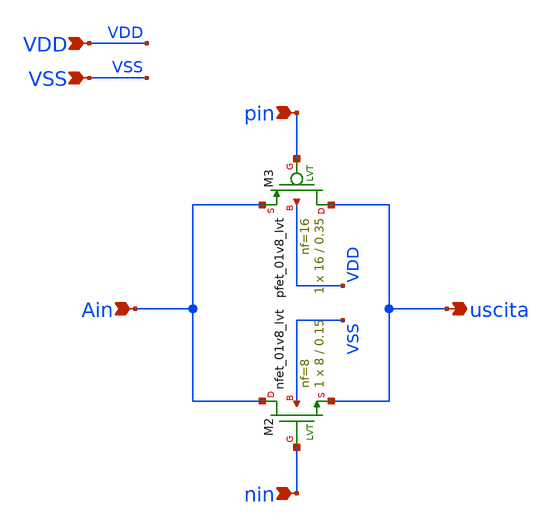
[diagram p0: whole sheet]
** sch_path: xschem/pass_gate.sch
**.subckt pass_gate Ain pin nin VDD VSS uscita
*.ipin Ain
*.ipin pin
*.ipin nin
*.ipin VDD
*.ipin VSS
*.opin uscita
XM2 Ain nin uscita VSS sky130_fd_pr__nfet_01v8_lvt L=0.15 W=8 nf=8 ad='int((nf+1)/2) * W/nf * 0.29' as='int((nf+2)/2) * W/nf * 0.29'
+ pd='2*int((nf+1)/2) * (W/nf + 0.29)' ps='2*int((nf+2)/2) * (W/nf + 0.29)' nrd='0.29 / W' nrs='0.29 / W'
+ sa=0 sb=0 sd=0 mult=1 m=1
XM3 uscita pin Ain VDD sky130_fd_pr__pfet_01v8_lvt L=0.35 W=16 nf=16 ad='int((nf+1)/2) * W/nf * 0.29'
+ as='int((nf+2)/2) * W/nf * 0.29' pd='2*int((nf+1)/2) * (W/nf + 0.29)' ps='2*int((nf+2)/2) * (W/nf + 0.29)'
+ nrd='0.29 / W' nrs='0.29 / W' sa=0 sb=0 sd=0 mult=1 m=1
**.ends
.end
